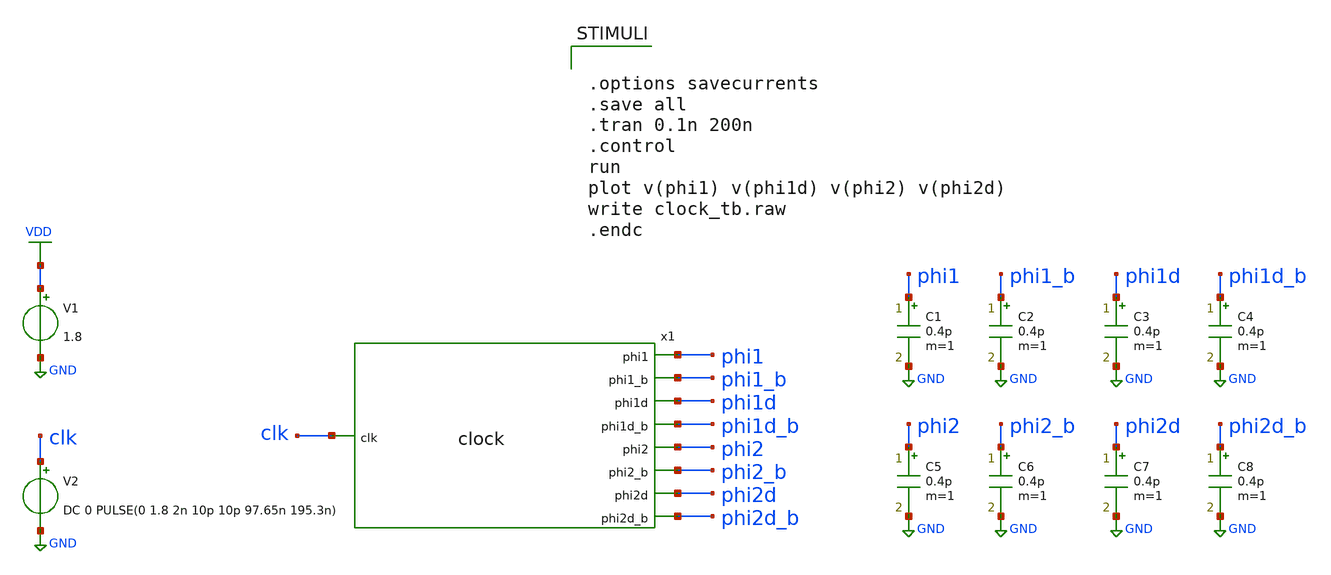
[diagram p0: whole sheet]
** sch_path: design/schematic/clock_tb.sch
**.subckt clock_tb
x1 clk phi1 phi1_b phi1d phi1d_b phi2 phi2_b phi2d phi2d_b clock
C1 phi1 GND 0.4p m=1
C2 phi1_b GND 0.4p m=1
C3 phi1d GND 0.4p m=1
C4 phi1d_b GND 0.4p m=1
C5 phi2 GND 0.4p m=1
C6 phi2_b GND 0.4p m=1
C7 phi2d GND 0.4p m=1
C8 phi2d_b GND 0.4p m=1
V1 VDD GND 1.8
V2 clk GND DC 0 PULSE(0 1.8 2n 10p 10p 97.65n 195.3n)
**** begin user architecture code


.options savecurrents
.save all
.tran 0.1n 200n
.control
run
plot v(phi1) v(phi1d) v(phi2) v(phi2d)
write clock_tb.raw
.endc



** opencircuitdesign pdks install
.lib /farmshare/home/classes/ee/372/PDKs/open_pdks_1.0.310/sky130/sky130A/libs.tech/ngspice/sky130.lib.spice tt

**** end user architecture code
**.ends

* expanding   symbol:  clock.sym # of pins=9
** sym_path: design/schematic/clock.sym
** sch_path: design/schematic/clock.sch
.subckt clock clk phi1 phi1_b phi1d phi1d_b phi2 phi2_b phi2d phi2d_b
*.opin phi1
*.opin phi1_b
*.opin phi1d
*.opin phi1d_b
*.opin phi2
*.opin phi2_b
*.opin phi2d
*.opin phi2d_b
*.ipin clk
x3 phi1 phi1_b VDD GND 1 4 0.2 10 0.2 inv
x1 phi1_b net2 VDD GND 1 4 0.2 10 0.2 inv
x2 phi1d phi1d_b VDD GND 1 4 0.2 10 0.2 inv
x5 phi2 phi2_b VDD GND 1 4 0.2 10 0.2 inv
x6 phi2_b net4 VDD GND 1 4 0.2 10 0.2 inv
x8 phi2d phi2d_b VDD GND 1 4 0.2 10 0.2 inv
x9 clk net7 VDD GND 1 4 0.2 10 0.2 inv
x12 clk net6 net1 VDD GND 1 4 0.2 10 0.2 nor2
x13 net5 net7 net3 VDD GND 1 4 0.2 10 0.2 nor2
x14 net1 net8 VDD GND 1 4 0.2 10 0.2 inv
x16 net8 phi1 VDD GND 1 4 0.2 10 0.2 inv
x17 net2 net9 VDD GND 1 4 0.2 10 0.2 inv
x18 net9 phi1d VDD GND 1 4 0.2 10 0.2 inv
x19 net3 net10 VDD GND 1 4 0.2 10 0.2 inv
x20 net10 phi2 VDD GND 1 4 0.2 10 0.2 inv
x21 net4 net11 VDD GND 1 4 0.2 10 0.2 inv
x24 net11 phi2d VDD GND 1 4 0.2 10 0.2 inv
x25 net23 net12 VDD GND 1 4 0.2 10 0.2 inv
x28 net12 net13 VDD GND 1 4 0.2 10 0.2 inv
x29 net13 net14 VDD GND 1 4 0.2 10 0.2 inv
x30 net16 net6 VDD GND 1 4 0.2 10 0.2 inv
x31 net14 net15 VDD GND 1 4 0.2 10 0.2 inv
x32 net15 net16 VDD GND 1 4 0.2 10 0.2 inv
x33 net22 net17 VDD GND 1 4 0.2 10 0.2 inv
x34 net17 net18 VDD GND 1 4 0.2 10 0.2 inv
x35 net18 net19 VDD GND 1 4 0.2 10 0.2 inv
x38 net21 net5 VDD GND 1 4 0.2 10 0.2 inv
x39 net19 net20 VDD GND 1 4 0.2 10 0.2 inv
x42 net20 net21 VDD GND 1 4 0.2 10 0.2 inv
x46 net29 net24 VDD GND 1 4 0.2 10 0.2 inv
x47 net24 net25 VDD GND 1 4 0.2 10 0.2 inv
x48 net25 net26 VDD GND 1 4 0.2 10 0.2 inv
x49 net28 net23 VDD GND 1 4 0.2 10 0.2 inv
x50 net26 net27 VDD GND 1 4 0.2 10 0.2 inv
x51 net27 net28 VDD GND 1 4 0.2 10 0.2 inv
x52 phi2d net30 VDD GND 1 4 0.2 10 0.2 inv
x53 net30 net29 VDD GND 1 4 0.2 10 0.2 inv
x54 net36 net31 VDD GND 1 4 0.2 10 0.2 inv
x55 net31 net32 VDD GND 1 4 0.2 10 0.2 inv
x56 net32 net33 VDD GND 1 4 0.2 10 0.2 inv
x57 net35 net22 VDD GND 1 4 0.2 10 0.2 inv
x58 net33 net34 VDD GND 1 4 0.2 10 0.2 inv
x59 net34 net35 VDD GND 1 4 0.2 10 0.2 inv
x60 phi1d net37 VDD GND 1 4 0.2 10 0.2 inv
x61 net37 net36 VDD GND 1 4 0.2 10 0.2 inv
.ends


* expanding   symbol:  inv.sym # of pins=2
** sym_path: design/schematic/inv.sym
** sch_path: design/schematic/inv.sch
.subckt inv in out VDD VSS N W_N L_N W_P L_P    N=1 W_N=2 L_N=0.2 W_P=5 L_P=0.2
*.ipin in
*.opin out
XM2 out in VSS VSS sky130_fd_pr__nfet_01v8 L=L_N W=W_N nf=1 ad='int((nf+1)/2) * W/nf * 0.29' as='int((nf+2)/2) * W/nf * 0.29'
+ pd='2*int((nf+1)/2) * (W/nf + 0.29)' ps='2*int((nf+2)/2) * (W/nf + 0.29)' nrd='0.29 / W' nrs='0.29 / W'
+ sa=0 sb=0 sd=0 mult=N m=N
XM1 out in VDD VDD sky130_fd_pr__pfet_01v8 L=L_P W=W_P nf=1 ad='int((nf+1)/2) * W/nf * 0.29' as='int((nf+2)/2) * W/nf * 0.29'
+ pd='2*int((nf+1)/2) * (W/nf + 0.29)' ps='2*int((nf+2)/2) * (W/nf + 0.29)' nrd='0.29 / W' nrs='0.29 / W'
+ sa=0 sb=0 sd=0 mult=N m=N
.ends


* expanding   symbol:  nor2.sym # of pins=3
** sym_path: design/schematic/nor2.sym
** sch_path: design/schematic/nor2.sch
.subckt nor2 in_1 in_2 out VDD VSS N W_N L_N W_P L_P    N=1 W_N=4 L_N=0.15 W_P=10 L_P=0.15
*.ipin in_1
*.ipin in_2
*.opin out
XM1 out in_2 VSS VSS sky130_fd_pr__nfet_01v8 L=L_N W=W_N nf=1 ad='int((nf+1)/2) * W/nf * 0.29' as='int((nf+2)/2) * W/nf * 0.29'
+ pd='2*int((nf+1)/2) * (W/nf + 0.29)' ps='2*int((nf+2)/2) * (W/nf + 0.29)' nrd='0.29 / W' nrs='0.29 / W'
+ sa=0 sb=0 sd=0 mult=N m=N
XM2 out in_1 VSS VSS sky130_fd_pr__nfet_01v8 L=L_N W=W_N nf=1 ad='int((nf+1)/2) * W/nf * 0.29' as='int((nf+2)/2) * W/nf * 0.29'
+ pd='2*int((nf+1)/2) * (W/nf + 0.29)' ps='2*int((nf+2)/2) * (W/nf + 0.29)' nrd='0.29 / W' nrs='0.29 / W'
+ sa=0 sb=0 sd=0 mult=N m=N
XM3 out in_2 net1 VDD sky130_fd_pr__pfet_01v8 L=L_P W=W_P nf=1 ad='int((nf+1)/2) * W/nf * 0.29' as='int((nf+2)/2) * W/nf * 0.29'
+ pd='2*int((nf+1)/2) * (W/nf + 0.29)' ps='2*int((nf+2)/2) * (W/nf + 0.29)' nrd='0.29 / W' nrs='0.29 / W'
+ sa=0 sb=0 sd=0 mult=N m=N
XM4 net1 in_1 VDD VDD sky130_fd_pr__pfet_01v8 L=L_P W=W_P nf=1 ad='int((nf+1)/2) * W/nf * 0.29' as='int((nf+2)/2) * W/nf * 0.29'
+ pd='2*int((nf+1)/2) * (W/nf + 0.29)' ps='2*int((nf+2)/2) * (W/nf + 0.29)' nrd='0.29 / W' nrs='0.29 / W'
+ sa=0 sb=0 sd=0 mult=N m=N
.ends

.GLOBAL GND
.GLOBAL VDD
.end
